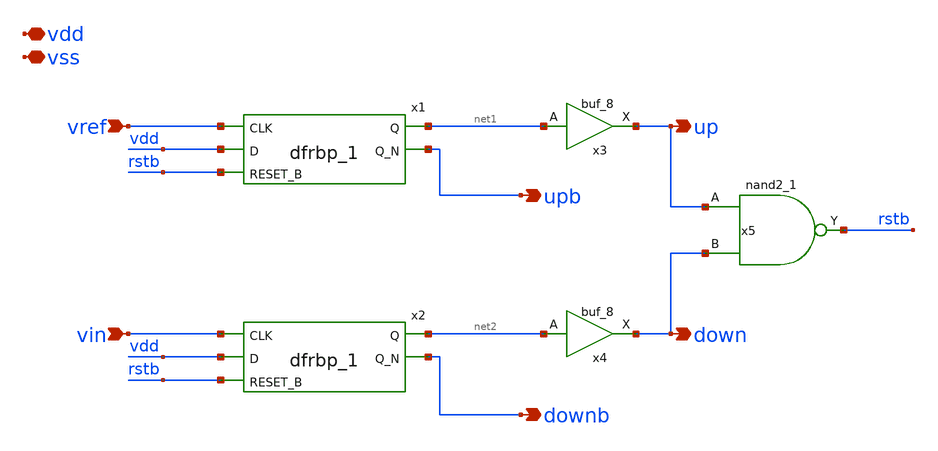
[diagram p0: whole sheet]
** sch_path: custom_gds/tt_um_mickey_pll/xschem/pfd.sch
**.subckt pfd vref vin vdd vss up down downb upb
*.ipin vref
*.ipin vin
*.iopin vdd
*.iopin vss
*.opin up
*.opin down
*.opin downb
*.opin upb
x1 vref vdd rstb vss vss vdd vdd net1 upb sky130_fd_sc_hd__dfrbp_1
x2 vin vdd rstb vss vss vdd vdd net2 downb sky130_fd_sc_hd__dfrbp_1
x3 net1 vss vss vdd vdd up sky130_fd_sc_hd__buf_8
x4 net2 vss vss vdd vdd down sky130_fd_sc_hd__buf_8
x5 up down vss vss vdd vdd rstb sky130_fd_sc_hd__nand2_1
**.ends
.end
